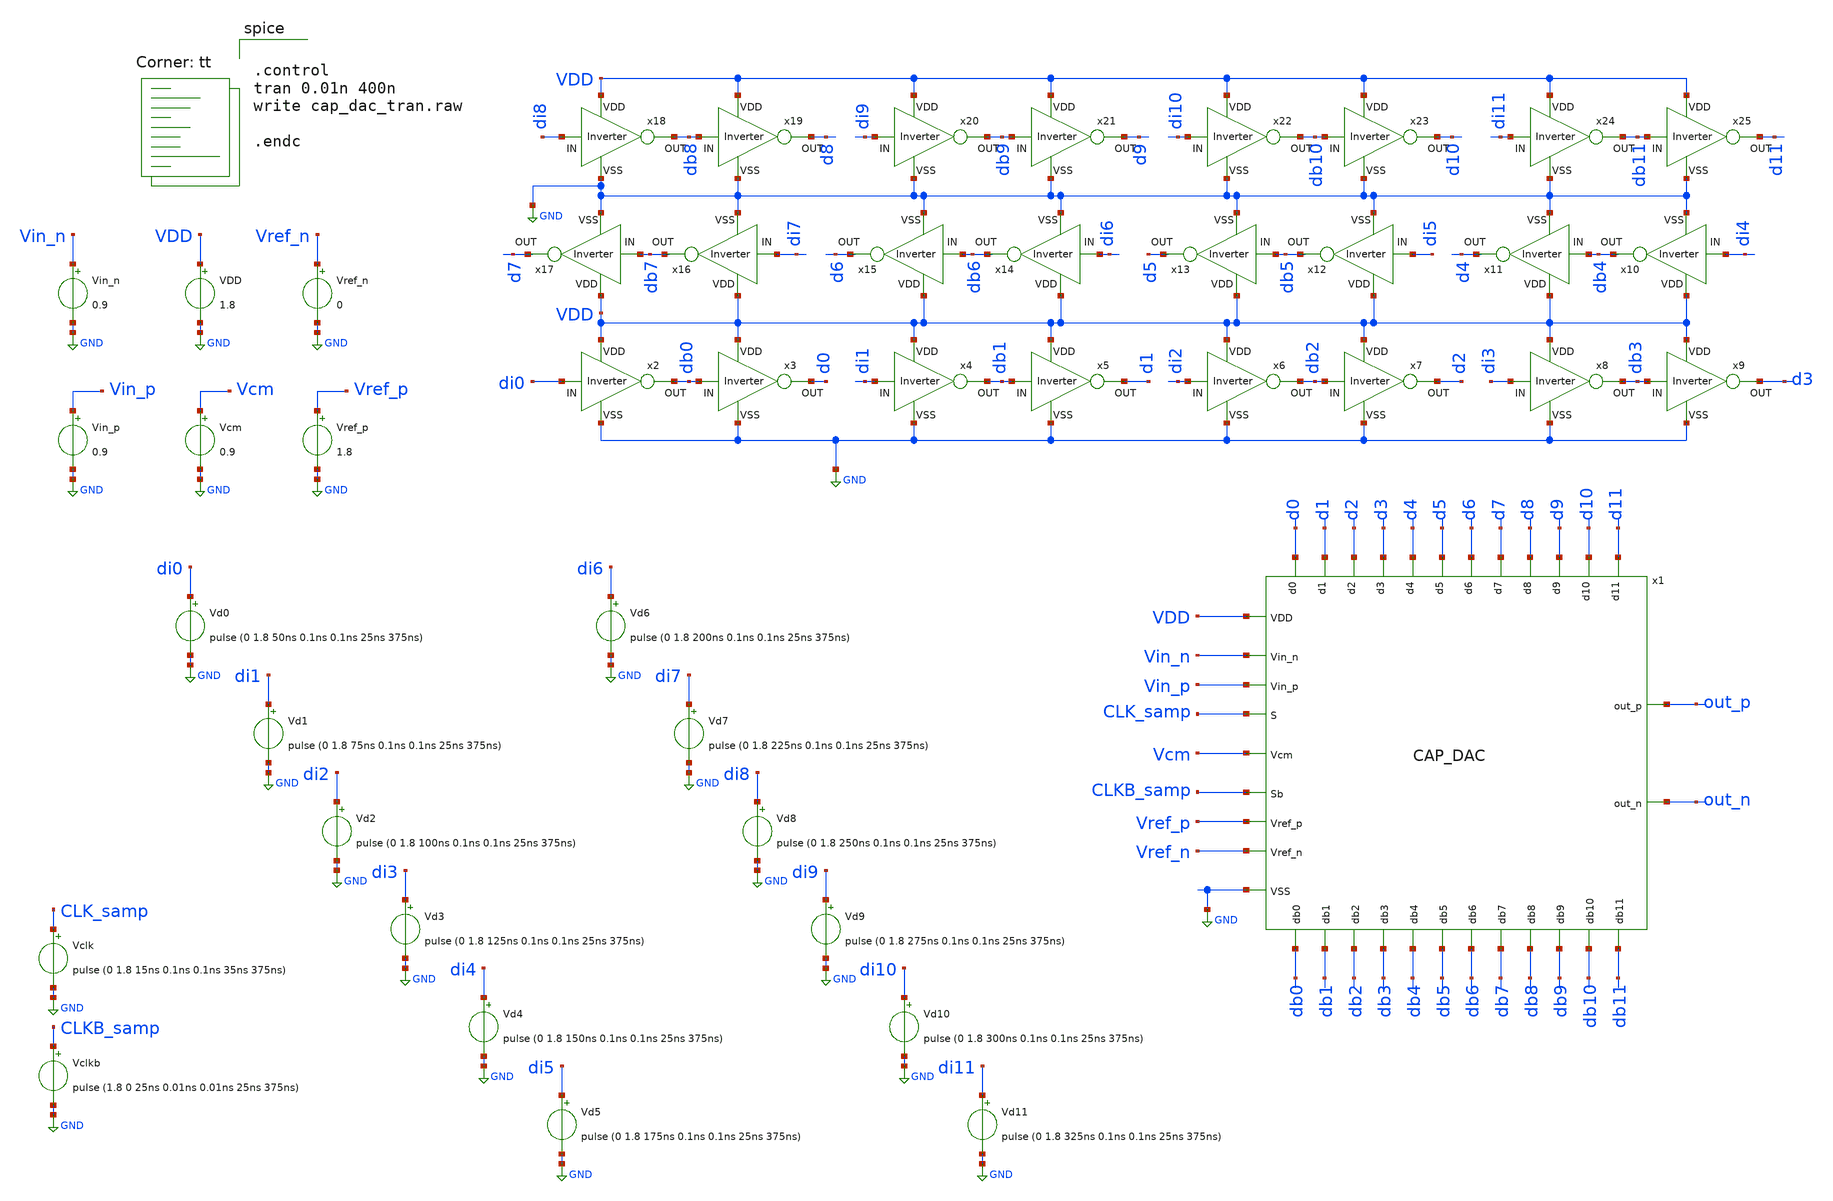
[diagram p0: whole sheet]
** sch_path: CAP_DAC_tb.sch
**.subckt CAP_DAC_tb
x1 Vref_n Vin_n db0 db1 db2 VDD d3 db3 GND db4 d4 out_p Vcm db5 d5 CLK_samp db6 d6 CLKB_samp db7 d7
+ out_n d8 db8 d9 db9 db10 d10 db11 d11 Vin_p Vref_p d0 d1 d2 CAP_DAC
x2 VDD di0 db0 GND Inverter
x3 VDD db0 d0 GND Inverter
x4 VDD di1 db1 GND Inverter
x5 VDD db1 d1 GND Inverter
x6 VDD di2 db2 GND Inverter
x7 VDD db2 d2 GND Inverter
x8 VDD di3 db3 GND Inverter
x9 VDD db3 d3 GND Inverter
x10 VDD di4 db4 GND Inverter
x11 VDD db4 d4 GND Inverter
x12 VDD di5 db5 GND Inverter
x13 VDD db5 d5 GND Inverter
x14 VDD di6 db6 GND Inverter
x15 VDD db6 d6 GND Inverter
x16 VDD di7 db7 GND Inverter
x17 VDD db7 d7 GND Inverter
x18 VDD di8 db8 GND Inverter
x19 VDD db8 d8 GND Inverter
x20 VDD di9 db9 GND Inverter
x21 VDD db9 d9 GND Inverter
x22 VDD di10 db10 GND Inverter
x23 VDD db10 d10 GND Inverter
x24 VDD di11 db11 GND Inverter
x25 VDD db11 d11 GND Inverter
VDD VDD GND 1.8
Vclk CLK_samp GND pulse (0 1.8 15ns 0.1ns 0.1ns 35ns 375ns)
Vclkb CLKB_samp GND pulse (1.8 0 25ns 0.01ns 0.01ns 25ns 375ns)
Vcm Vcm GND 0.9
Vin_n Vin_n GND 0.9
Vin_p Vin_p GND 0.9
Vref_n Vref_n GND 0
Vref_p Vref_p GND 1.8
Vd0 di0 GND pulse (0 1.8 50ns 0.1ns 0.1ns 25ns 375ns)
Vd1 di1 GND pulse (0 1.8 75ns 0.1ns 0.1ns 25ns 375ns)
Vd2 di2 GND pulse (0 1.8 100ns 0.1ns 0.1ns 25ns 375ns)
Vd3 di3 GND pulse (0 1.8 125ns 0.1ns 0.1ns 25ns 375ns)
Vd4 di4 GND pulse (0 1.8 150ns 0.1ns 0.1ns 25ns 375ns)
Vd5 di5 GND pulse (0 1.8 175ns 0.1ns 0.1ns 25ns 375ns)
Vd6 di6 GND pulse (0 1.8 200ns 0.1ns 0.1ns 25ns 375ns)
Vd7 di7 GND pulse (0 1.8 225ns 0.1ns 0.1ns 25ns 375ns)
Vd8 di8 GND pulse (0 1.8 250ns 0.1ns 0.1ns 25ns 375ns)
Vd9 di9 GND pulse (0 1.8 275ns 0.1ns 0.1ns 25ns 375ns)
Vd10 di10 GND pulse (0 1.8 300ns 0.1ns 0.1ns 25ns 375ns)
Vd11 di11 GND pulse (0 1.8 325ns 0.1ns 0.1ns 25ns 375ns)
**** begin user architecture code
.lib $::SKYWATER_MODELS/sky130.lib.spice tt


.control
tran 0.01n 400n
write cap_dac_tran.raw

.endc


**** end user architecture code
**.ends
.GLOBAL GND
.end
